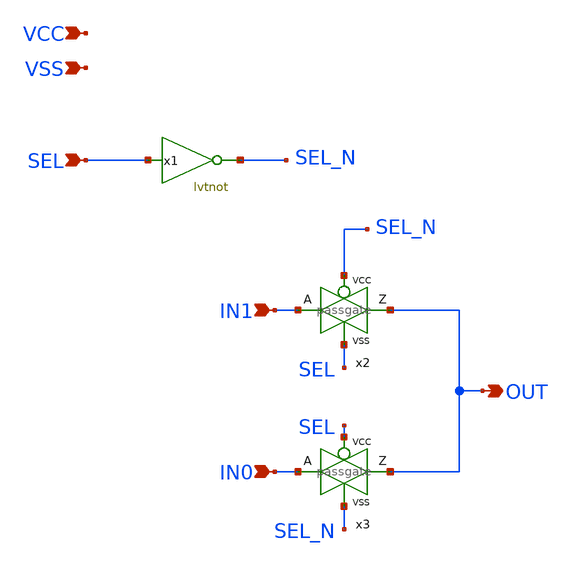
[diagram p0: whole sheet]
** sch_path: xschem/onehot2mux.sch
**.subckt onehot2mux SEL IN0 IN1 OUT VCC VSS
*.ipin SEL
*.ipin IN0
*.ipin IN1
*.opin OUT
*.ipin VCC
*.ipin VSS
x2 OUT IN1 SEL_N SEL VCC VSS passgate W_N=1 L_N=0.2 W_P=1 L_P=0.2 m=1
x3 OUT IN0 SEL SEL_N VCC VSS passgate W_N=1 L_N=0.2 W_P=1 L_P=0.2 m=1
x1 SEL SEL_N VCC VSS lvtnot W_N=1 L_N=0.15 W_P=2 L_P=0.35 m=1
**.ends
.end
